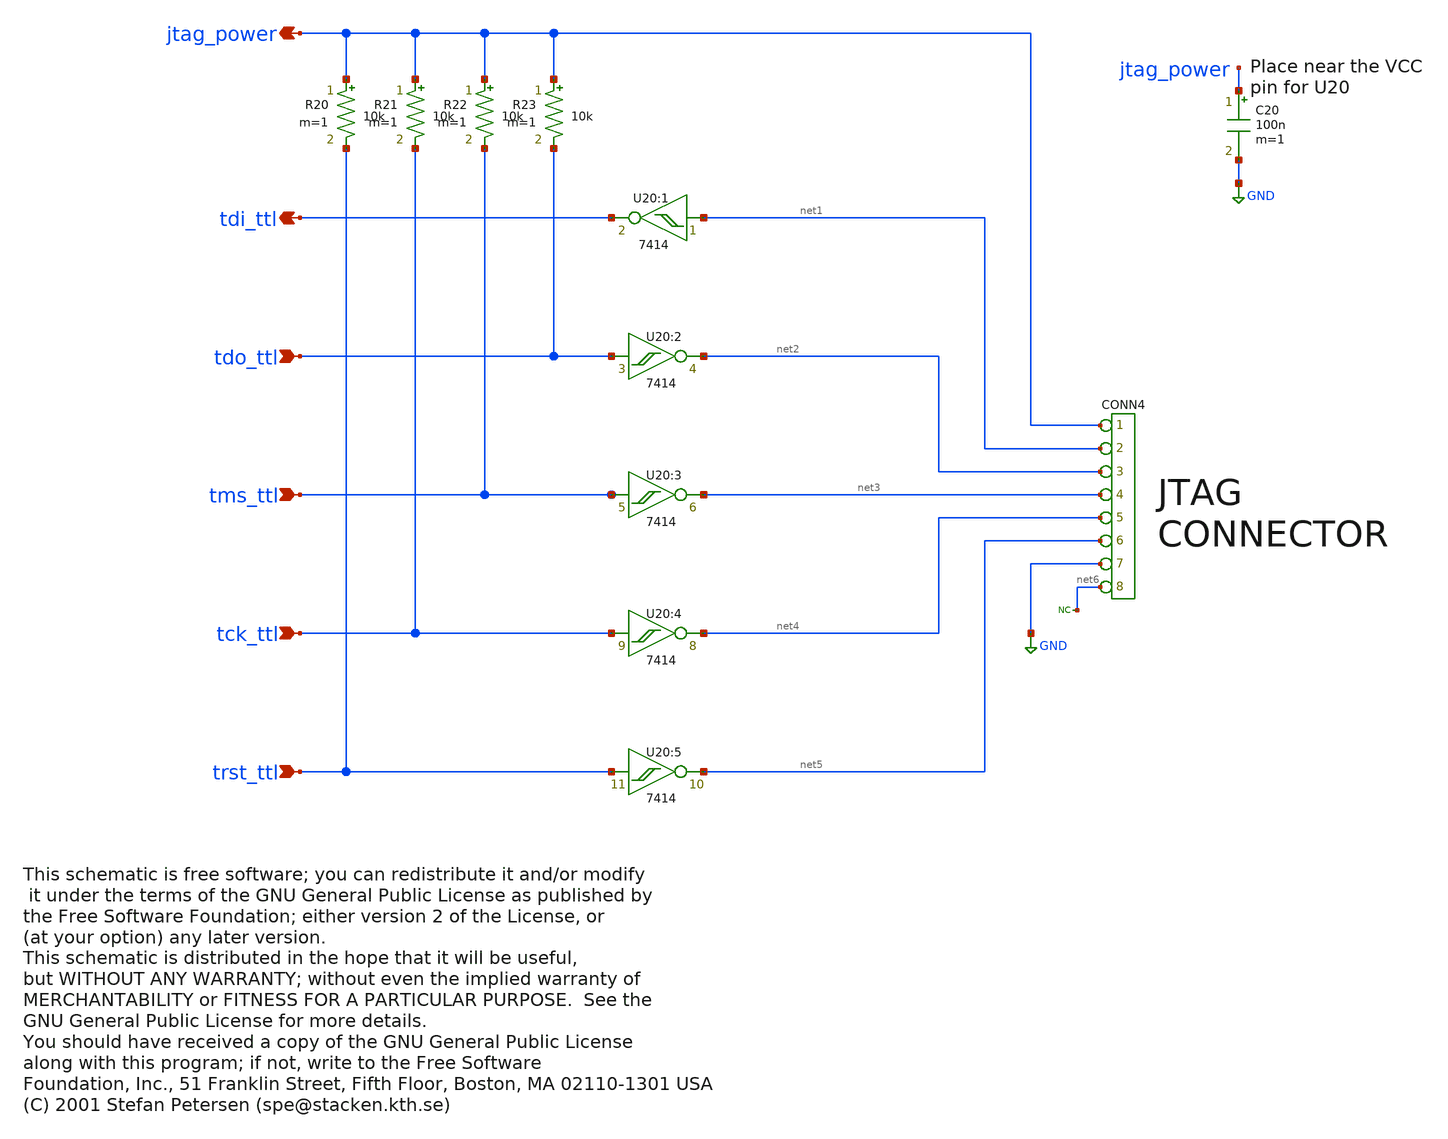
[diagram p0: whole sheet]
** sch_path: xschem_libraries_oa/xTAG/xTAG-jtagio/schematic/xTAG-jtagio.sch
* Copyright (C) 1998-2024 Stefan Frederik Schippers
* This program is free software; you can redistribute it and/or modify
* it under the terms of the GNU General Public License as published by
* the Free Software Foundation; either version 2 of the License, or
* (at your option) any later version.
* This program is distributed in the hope that it will be useful,
* but WITHOUT ANY WARRANTY; without even the implied warranty of
* MERCHANTABILITY or FITNESS FOR A PARTICULAR PURPOSE.  See the
* GNU General Public License for more details.
* You should have received a copy of the GNU General Public License
* along with this program; if not, write to the Free Software
* This schematic is free software; you can redistribute it and/or modify
* (C) 2001 Stefan Petersen (spe@stacken.kth.se)
**.subckt xTAG-jtagio jtag_power tdi_ttl tdo_ttl tms_ttl tck_ttl trst_ttl
*.opin jtag_power
*.opin tdi_ttl
*.ipin tdo_ttl
*.ipin tms_ttl
*.ipin tck_ttl
*.ipin trst_ttl
U20:1 net1 tdi_ttl m=
U20:2 tdo_ttl net2 m=
U20:3 tms_ttl net3 m=
U20:4 tck_ttl net4 m=
U20:5 trst_ttl net5 m=
*connector(8,1) ?1 jtag_power ?1 net1 ?1 net2 ?1 net3 ?1 net4 ?1 net5 ?1 GND ?1 net6
* noconn #net6
C20 jtag_power GND 100n m=1
R23 jtag_power tdo_ttl 10k m=1
R22 jtag_power tms_ttl 10k m=1
R21 jtag_power tck_ttl 10k m=1
R20 jtag_power trst_ttl 10k m=1
**.ends
.GLOBAL GND
.end
